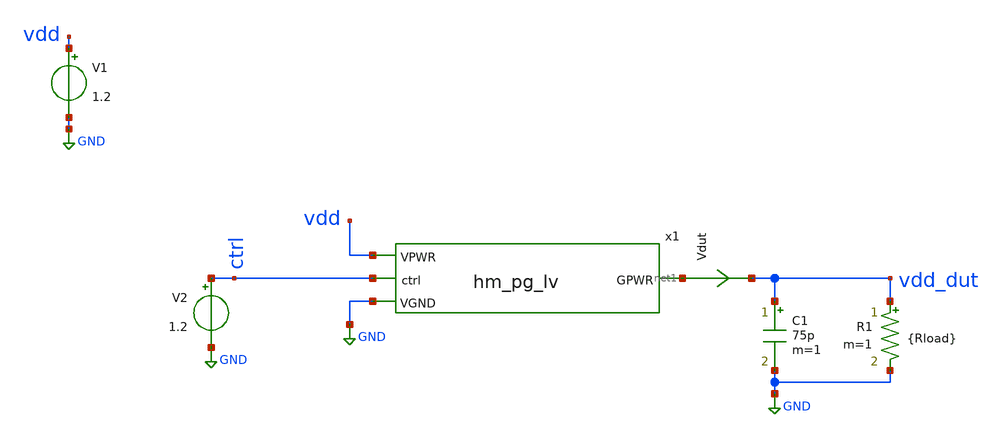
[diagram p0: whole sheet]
** sch_path: ihp-sg13cmos5l/libs.tech/xschem/tests/tb_hm_pg_lv.sch
**.subckt tb_hm_pg_lv
V1 vdd GND 1.2
.save i(v1)
V2 ctrl GND 1.2
C1 vdd_dut GND 75p m=1
Vdut net1 vdd_dut 0
.save i(vdut)
R1 vdd_dut GND {Rload} m=1
x1 vdd net1 ctrl GND hm_pg_lv
**** begin user architecture code

.lib cornerMOSlv.lib mos_tt
*.lib cornerCAP.lib cap_typ



.param Rload=1000

.control

let npoints = 8
let rvec = vector(npoints)
let ivec = vector(npoints)
let vdrop_vec = vector(npoints)
let ron_vec = vector(npoints)

let vdd_dutvec = vector(npoints)

let idx=0

foreach r 10000 5000 2000 1000 500 200 100 10
  alterparam Rload=$r
  reset
  save all
  op

  let iload = i(vdut)
  let vdrop = v(vdd) - v(vdd_dut)
  let ron = vdrop/iload

  let rvec[idx] = $r
  let ivec[idx] = iload
  let vdrop_vec[idx] = vdrop
  let ron_vec[idx] = ron

  let vdd_dutvec[idx] = vdd_dut

  echo -------------------------
  echo Rload = $r
  print iload vdrop ron

  let idx = idx + 1
end

plot ron_vec vs ivec
plot vdd_dutvec vs ivec

.endc


**** end user architecture code
**.ends

* expanding   symbol:
*+  /home/designer/shared/hm-openpdk-library/ihp-sg13cmos5l/libs.tech/xschem/hm_analog/hm_pg_lv.sym # of pins=4
** sym_path: ihp-sg13cmos5l/libs.tech/xschem/hm_analog/hm_pg_lv.sym
** sch_path: ihp-sg13cmos5l/libs.tech/xschem/hm_analog/hm_pg_lv.sch
.subckt hm_pg_lv VPWR GPWR ctrl VGND
*.ipin ctrl
*.iopin VPWR
*.iopin VGND
*.iopin GPWR
XM1 ctrl_n ctrl VGND VGND sg13_lv_nmos w=2.6u l=0.13u ng=1 m=1 mm_ok=1
XM2 ctrl_n ctrl VPWR VPWR sg13_lv_pmos w=4.44u l=0.13u ng=1 m=1 mm_ok=1
XM3 GPWR ctrl_n VPWR VPWR sg13_lv_pmos w=2175u l=0.13u ng=290 m=1 mm_ok=1
x1 VGND GPWR ctrl_n dischg
.ends


* expanding   symbol:  hm_analog/dischg.sym # of pins=3
** sym_path: ihp-sg13cmos5l/libs.tech/xschem/hm_analog/dischg.sym
** sch_path: ihp-sg13cmos5l/libs.tech/xschem/hm_analog/dischg.sch
.subckt dischg VGND GPWR gate
*.iopin GPWR
*.iopin VGND
*.ipin gate
XM1 GPWR gate net2 VGND sg13_lv_nmos w=4u l=0.65u ng=1 m=1 mm_ok=1
XM2 net2 gate net3 VGND sg13_lv_nmos w=4u l=0.65u ng=1 m=1 mm_ok=1
XM3 net3 gate net4 VGND sg13_lv_nmos w=4u l=0.65u ng=1 m=1 mm_ok=1
XM4 net4 gate net1 VGND sg13_lv_nmos w=4u l=0.65u ng=1 m=1 mm_ok=1
XM5 net1 gate net7 VGND sg13_lv_nmos w=4u l=0.65u ng=1 m=1 mm_ok=1
XM6 net7 gate net6 VGND sg13_lv_nmos w=4u l=0.65u ng=1 m=1 mm_ok=1
XM7 net6 gate net5 VGND sg13_lv_nmos w=4u l=0.65u ng=1 m=1 mm_ok=1
XM8 net5 gate VGND VGND sg13_lv_nmos w=4u l=0.65u ng=1 m=1 mm_ok=1
XM9 GPWR gate net9 VGND sg13_lv_nmos w=4u l=0.65u ng=1 m=1 mm_ok=1
XM10 net9 gate net10 VGND sg13_lv_nmos w=4u l=0.65u ng=1 m=1 mm_ok=1
XM11 net10 gate net11 VGND sg13_lv_nmos w=4u l=0.65u ng=1 m=1 mm_ok=1
XM12 net11 gate net8 VGND sg13_lv_nmos w=4u l=0.65u ng=1 m=1 mm_ok=1
XM13 net8 gate net14 VGND sg13_lv_nmos w=4u l=0.65u ng=1 m=1 mm_ok=1
XM14 net14 gate net13 VGND sg13_lv_nmos w=4u l=0.65u ng=1 m=1 mm_ok=1
XM15 net13 gate net12 VGND sg13_lv_nmos w=4u l=0.65u ng=1 m=1 mm_ok=1
XM16 net12 gate VGND VGND sg13_lv_nmos w=4u l=0.65u ng=1 m=1 mm_ok=1
.ends

.GLOBAL GND
.end
